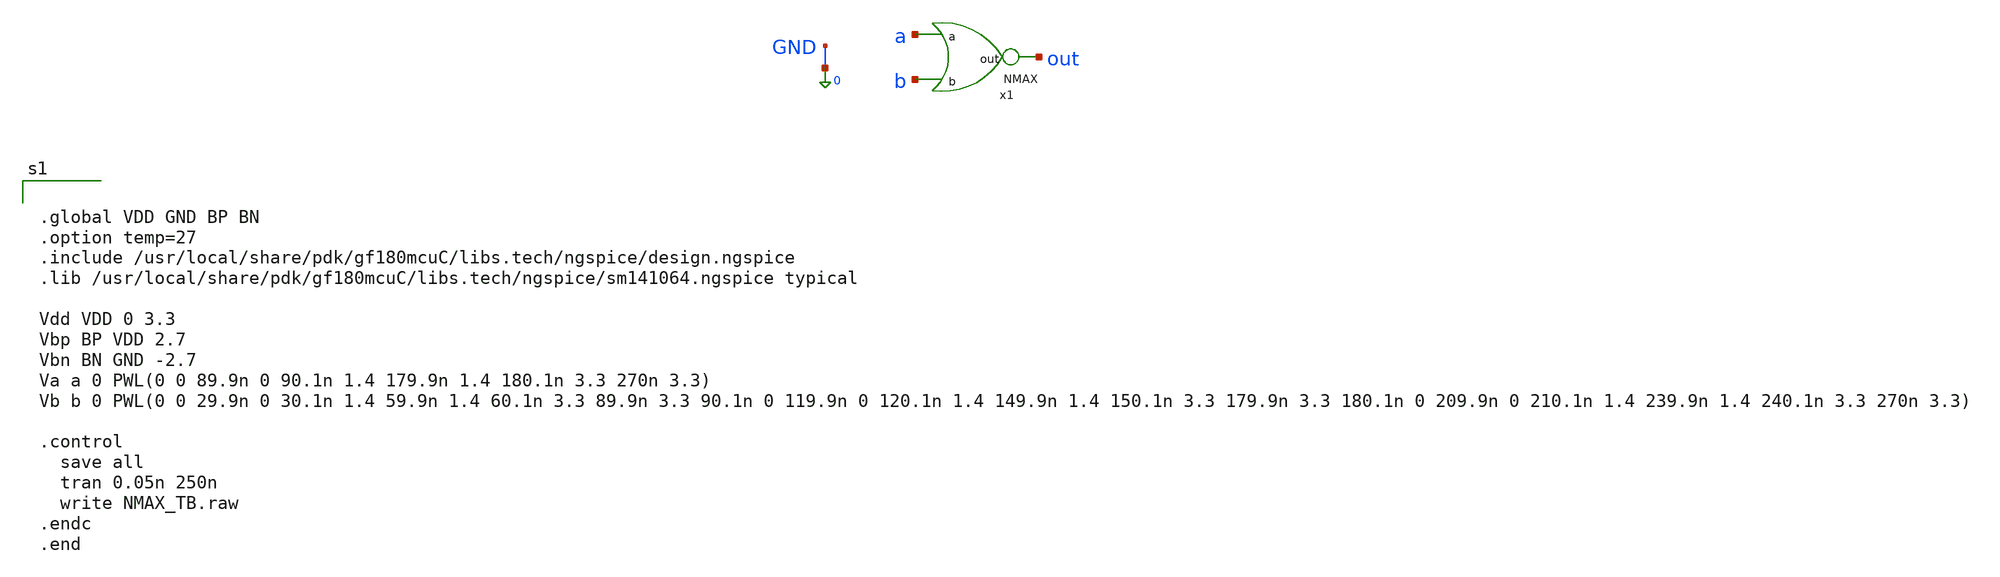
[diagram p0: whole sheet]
** sch_path: xschem_designs/NMAX_TB.sch
**.subckt NMAX_TB
x1 out a b NMAX
**** begin user architecture code


.global VDD GND BP BN
.option temp=27
.include /usr/local/share/pdk/gf180mcuC/libs.tech/ngspice/design.ngspice
.lib /usr/local/share/pdk/gf180mcuC/libs.tech/ngspice/sm141064.ngspice typical

Vdd VDD 0 3.3
Vbp BP VDD 2.7
Vbn BN GND -2.7
Va a 0 PWL(0 0 89.9n 0 90.1n 1.4 179.9n 1.4 180.1n 3.3 270n 3.3)
Vb b 0 PWL(0 0 29.9n 0 30.1n 1.4 59.9n 1.4 60.1n 3.3 89.9n 3.3 90.1n 0 119.9n 0 120.1n 1.4 149.9n
+ 1.4 150.1n 3.3 179.9n 3.3 180.1n 0 209.9n 0 210.1n 1.4 239.9n 1.4 240.1n 3.3 270n 3.3)

.control
  save all
  tran 0.05n 250n
  write NMAX_TB.raw
.endc
.end


**** end user architecture code
**.ends

* expanding   symbol:  xschem_designs/NMAX.sym # of pins=3
** sym_path: xschem_designs/NMAX.sym
** sch_path: xschem_designs/NMAX.sch
.subckt NMAX out a b
*.ipin a
*.ipin b
*.opin out
XM13 out out net1 GND nfet_03v3 L=2.24u W=0.22u nf=1 ad='int((nf+1)/2) * W/nf * 0.18u' as='int((nf+2)/2) * W/nf * 0.18u'
+ pd='2*int((nf+1)/2) * (W/nf + 0.18u)' ps='2*int((nf+2)/2) * (W/nf + 0.18u)' nrd='0.18u / W' nrs='0.18u / W'
+ sa=0 sb=0 sd=0 m=1 par=1
XM14 out a GND BN nfet_06v0 L=1.4u W=0.30u nf=1 ad='int((nf+1)/2) * W/nf * 0.18u' as='int((nf+2)/2) * W/nf * 0.18u'
+ pd='2*int((nf+1)/2) * (W/nf + 0.18u)' ps='2*int((nf+2)/2) * (W/nf + 0.18u)' nrd='0.18u / W' nrs='0.18u / W'
+ sa=0 sb=0 sd=0 m=1 par=1
XM15 out b GND BN nfet_06v0 L=1.4u W=0.30u nf=1 ad='int((nf+1)/2) * W/nf * 0.18u' as='int((nf+2)/2) * W/nf * 0.18u'
+ pd='2*int((nf+1)/2) * (W/nf + 0.18u)' ps='2*int((nf+2)/2) * (W/nf + 0.18u)' nrd='0.18u / W' nrs='0.18u / W'
+ sa=0 sb=0 sd=0 m=1 par=1
XM18 net1 a GND GND nfet_03v3 L=0.28u W=0.22u nf=1 ad='int((nf+1)/2) * W/nf * 0.18u' as='int((nf+2)/2) * W/nf * 0.18u'
+ pd='2*int((nf+1)/2) * (W/nf + 0.18u)' ps='2*int((nf+2)/2) * (W/nf + 0.18u)' nrd='0.18u / W' nrs='0.18u / W'
+ sa=0 sb=0 sd=0 m=1 par=1
XM19 net1 b GND GND nfet_03v3 L=0.28u W=0.22u nf=1 ad='int((nf+1)/2) * W/nf * 0.18u' as='int((nf+2)/2) * W/nf * 0.18u'
+ pd='2*int((nf+1)/2) * (W/nf + 0.18u)' ps='2*int((nf+2)/2) * (W/nf + 0.18u)' nrd='0.18u / W' nrs='0.18u / W'
+ sa=0 sb=0 sd=0 m=1 par=1
XM11 net2 a VDD VDD pfet_03v3 L=0.28u W=0.44u nf=1 ad='int((nf+1)/2) * W/nf * 0.18u' as='int((nf+2)/2) * W/nf * 0.18u'
+ pd='2*int((nf+1)/2) * (W/nf + 0.18u)' ps='2*int((nf+2)/2) * (W/nf + 0.18u)' nrd='0.18u / W' nrs='0.18u / W'
+ sa=0 sb=0 sd=0 m=1 par=1
XM12 out out net3 VDD pfet_03v3 L=1.12u W=0.22u nf=1 ad='int((nf+1)/2) * W/nf * 0.18u' as='int((nf+2)/2) * W/nf * 0.18u'
+ pd='2*int((nf+1)/2) * (W/nf + 0.18u)' ps='2*int((nf+2)/2) * (W/nf + 0.18u)' nrd='0.18u / W' nrs='0.18u / W'
+ sa=0 sb=0 sd=0 m=1 par=1
XM16 net4 a VDD BP pfet_06v0 L=1.1u W=0.60u nf=1 ad='int((nf+1)/2) * W/nf * 0.18u' as='int((nf+2)/2) * W/nf * 0.18u'
+ pd='2*int((nf+1)/2) * (W/nf + 0.18u)' ps='2*int((nf+2)/2) * (W/nf + 0.18u)' nrd='0.18u / W' nrs='0.18u / W'
+ sa=0 sb=0 sd=0 m=1 par=1
XM17 out b net4 BP pfet_06v0 L=1.1u W=0.60u nf=1 ad='int((nf+1)/2) * W/nf * 0.18u' as='int((nf+2)/2) * W/nf * 0.18u'
+ pd='2*int((nf+1)/2) * (W/nf + 0.18u)' ps='2*int((nf+2)/2) * (W/nf + 0.18u)' nrd='0.18u / W' nrs='0.18u / W'
+ sa=0 sb=0 sd=0 m=1 par=1
XM20 net3 b net2 VDD pfet_03v3 L=0.28u W=0.44u nf=1 ad='int((nf+1)/2) * W/nf * 0.18u' as='int((nf+2)/2) * W/nf * 0.18u'
+ pd='2*int((nf+1)/2) * (W/nf + 0.18u)' ps='2*int((nf+2)/2) * (W/nf + 0.18u)' nrd='0.18u / W' nrs='0.18u / W'
+ sa=0 sb=0 sd=0 m=1 par=1
.ends

.end
